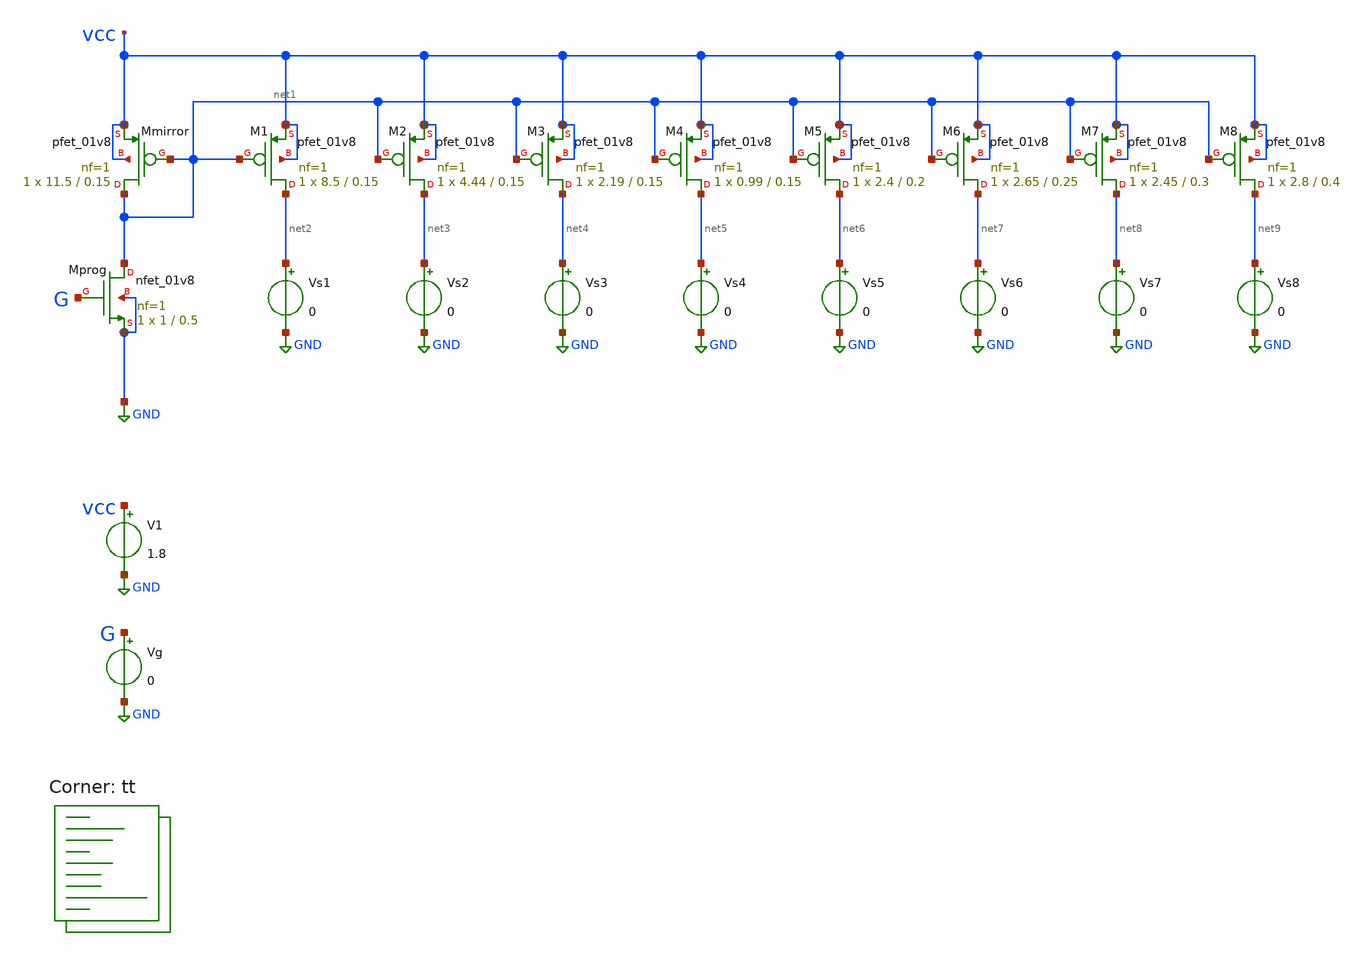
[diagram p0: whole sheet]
** sch_path: xschem/04-csdac1.sch
**.subckt 04-csdac1
V1 vcc GND 1.8
Vg G GND 0
XMprog net1 G GND GND sky130_fd_pr__nfet_01v8 L=0.5 W=1 nf=1 ad='int((nf+1)/2) * W/nf * 0.29' as='int((nf+2)/2) * W/nf * 0.29'
+ pd='2*int((nf+1)/2) * (W/nf + 0.29)' ps='2*int((nf+2)/2) * (W/nf + 0.29)' nrd='0.29 / W' nrs='0.29 / W'
+ sa=0 sb=0 sd=0 mult=1 m=1
XMmirror net1 net1 vcc vcc sky130_fd_pr__pfet_01v8 L=0.15 W=11.5 nf=1 ad='int((nf+1)/2) * W/nf * 0.29'
+ as='int((nf+2)/2) * W/nf * 0.29' pd='2*int((nf+1)/2) * (W/nf + 0.29)' ps='2*int((nf+2)/2) * (W/nf + 0.29)'
+ nrd='0.29 / W' nrs='0.29 / W' sa=0 sb=0 sd=0 mult=1 m=1
XM1 net2 net1 vcc vcc sky130_fd_pr__pfet_01v8 L=0.15 W=8.5 nf=1 ad='int((nf+1)/2) * W/nf * 0.29' as='int((nf+2)/2) * W/nf * 0.29'
+ pd='2*int((nf+1)/2) * (W/nf + 0.29)' ps='2*int((nf+2)/2) * (W/nf + 0.29)' nrd='0.29 / W' nrs='0.29 / W'
+ sa=0 sb=0 sd=0 mult=1 m=1
Vs1 net2 GND 0
XM2 net3 net1 vcc vcc sky130_fd_pr__pfet_01v8 L=0.15 W=4.44 nf=1 ad='int((nf+1)/2) * W/nf * 0.29' as='int((nf+2)/2) * W/nf * 0.29'
+ pd='2*int((nf+1)/2) * (W/nf + 0.29)' ps='2*int((nf+2)/2) * (W/nf + 0.29)' nrd='0.29 / W' nrs='0.29 / W'
+ sa=0 sb=0 sd=0 mult=1 m=1
Vs2 net3 GND 0
XM3 net4 net1 vcc vcc sky130_fd_pr__pfet_01v8 L=0.15 W=2.19 nf=1 ad='int((nf+1)/2) * W/nf * 0.29' as='int((nf+2)/2) * W/nf * 0.29'
+ pd='2*int((nf+1)/2) * (W/nf + 0.29)' ps='2*int((nf+2)/2) * (W/nf + 0.29)' nrd='0.29 / W' nrs='0.29 / W'
+ sa=0 sb=0 sd=0 mult=1 m=1
Vs3 net4 GND 0
XM4 net5 net1 vcc vcc sky130_fd_pr__pfet_01v8 L=0.15 W=0.99 nf=1 ad='int((nf+1)/2) * W/nf * 0.29' as='int((nf+2)/2) * W/nf * 0.29'
+ pd='2*int((nf+1)/2) * (W/nf + 0.29)' ps='2*int((nf+2)/2) * (W/nf + 0.29)' nrd='0.29 / W' nrs='0.29 / W'
+ sa=0 sb=0 sd=0 mult=1 m=1
Vs4 net5 GND 0
XM5 net6 net1 vcc vcc sky130_fd_pr__pfet_01v8 L=0.2 W=2.4 nf=1 ad='int((nf+1)/2) * W/nf * 0.29' as='int((nf+2)/2) * W/nf * 0.29'
+ pd='2*int((nf+1)/2) * (W/nf + 0.29)' ps='2*int((nf+2)/2) * (W/nf + 0.29)' nrd='0.29 / W' nrs='0.29 / W'
+ sa=0 sb=0 sd=0 mult=1 m=1
Vs5 net6 GND 0
XM6 net7 net1 vcc vcc sky130_fd_pr__pfet_01v8 L=0.25 W=2.65 nf=1 ad='int((nf+1)/2) * W/nf * 0.29' as='int((nf+2)/2) * W/nf * 0.29'
+ pd='2*int((nf+1)/2) * (W/nf + 0.29)' ps='2*int((nf+2)/2) * (W/nf + 0.29)' nrd='0.29 / W' nrs='0.29 / W'
+ sa=0 sb=0 sd=0 mult=1 m=1
Vs6 net7 GND 0
XM7 net8 net1 vcc vcc sky130_fd_pr__pfet_01v8 L=0.3 W=2.45 nf=1 ad='int((nf+1)/2) * W/nf * 0.29' as='int((nf+2)/2) * W/nf * 0.29'
+ pd='2*int((nf+1)/2) * (W/nf + 0.29)' ps='2*int((nf+2)/2) * (W/nf + 0.29)' nrd='0.29 / W' nrs='0.29 / W'
+ sa=0 sb=0 sd=0 mult=1 m=1
Vs7 net8 GND 0
XM8 net9 net1 vcc vcc sky130_fd_pr__pfet_01v8 L=0.4 W=2.8 nf=1 ad='int((nf+1)/2) * W/nf * 0.29' as='int((nf+2)/2) * W/nf * 0.29'
+ pd='2*int((nf+1)/2) * (W/nf + 0.29)' ps='2*int((nf+2)/2) * (W/nf + 0.29)' nrd='0.29 / W' nrs='0.29 / W'
+ sa=0 sb=0 sd=0 mult=1 m=1
Vs8 net9 GND 0
**** begin user architecture code



.DC Vg 0 1.8 0.01

*.param GW     = 0.5
*.param GL     = 0.15

.options savecurrents
.control

  let gwstart = 0.5
  let gwstep  = 0.05
  let gwi     = gwstart

  repeat 1
    set gwvar=$&gwi
    *echo Gate width = $gwvar
    *alterparam GW = $gwvar
    save all
    run
    write 04.raw G i(Vs1) i(Vs2) i(Vs3) i(Vs4) i(Vs5) i(Vs6) i(Vs7) i(Vs8)
    *+ i(Vs0p15) i(Vs0p25) i(Vs0p35) i(Vs0p50)
    *set appendwrite
    *reset
    *let gwi = gwi + gwstep
  end

.endc



.lib $::SKYWATER_MODELS/sky130.lib.spice tt
**** end user architecture code
**.ends
.GLOBAL GND
.end
